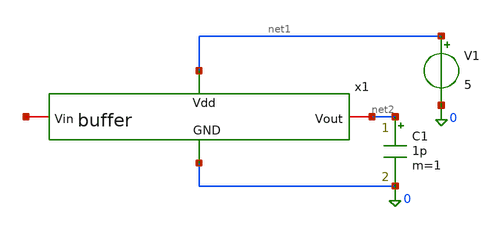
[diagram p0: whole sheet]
** sch_path: RN_buffer/buffer_testbench.sch
**.subckt buffer_testbench
V1 net1 0 5
C1 net2 0 1p m=1
x1 net1 net2 net3 0 buffer
**** begin user architecture code


Vin_src net3 0 DC 2.5 AC 1 PULSE(2.0 3.0 0n 1n 1n 0.5u 1u)

.include /foss/pdks/gf180mcuD/libs.tech/ngspice/design.ngspice
.lib /foss/pdks/gf180mcuD/libs.tech/ngspice/sm141064.ngspice typical
.lib /foss/pdks/gf180mcuD/libs.tech/ngspice/sm141064.ngspice res_typical
.lib /foss/pdks/gf180mcuD/libs.tech/ngspice/sm141064.ngspice moscap_typical
.lib /foss/pdks/gf180mcuD/libs.tech/ngspice/sm141064.ngspice diode_typical

.control
  save all

  * --- 1. RUN AC SWEEP (Bode Plot) ---
  ac dec 20 1 100Meg
  set units = degrees
  plot vdb(net2) vs frequency title 'Buffer AC Magnitude (dB)'
  plot cph(net2) vs frequency title 'Buffer Phase Response (Degrees)'

  * --- 2. RUN TRANSIENT ANALYSIS (1MHz Speed Check) ---
  tran 1n 5u
  plot v(net3) v(net2) title '1MHz Transient Response: Vin (net3) vs Vout (net2)'

  write buffer_results.raw
.endc

.options savecurrents


**** end user architecture code
**.ends

* expanding   symbol:  C05-MRTMOS-SSCS-Chipathon/RN_buffer/buffer.sym # of pins=4
** sym_path: RN_buffer/buffer.sym
** sch_path: RN_buffer/buffer.sch
.subckt buffer Vdd Vout Vin GND
*.ipin Vdd
*.ipin GND
*.iopin Vin
*.iopin Vout
XM1 GND Vin Vout Vout pfet_05v0 L=1u W=30u nf=10 ad='int((nf+1)/2) * W/nf * 0.18u' as='int((nf+2)/2) * W/nf * 0.18u'
+ pd='2*int((nf+1)/2) * (W/nf + 0.18u)' ps='2*int((nf+2)/2) * (W/nf + 0.18u)' nrd='0.18u / W' nrs='0.18u / W'
+ sa=0 sb=0 sd=0 m=2
XR1 net1 Vdd GND ppolyf_u_3k r_width=1e-6 r_length=150e-6 m=1
XR2 GND net1 GND ppolyf_u_3k r_width=1e-6 r_length=350e-6 m=1
XM2 Vout net1 Vdd Vdd pfet_05v0 L=1.2u W=16u nf=8 ad='int((nf+1)/2) * W/nf * 0.18u' as='int((nf+2)/2) * W/nf * 0.18u'
+ pd='2*int((nf+1)/2) * (W/nf + 0.18u)' ps='2*int((nf+2)/2) * (W/nf + 0.18u)' nrd='0.18u / W' nrs='0.18u / W'
+ sa=0 sb=0 sd=0 m=1
.ends

.end
